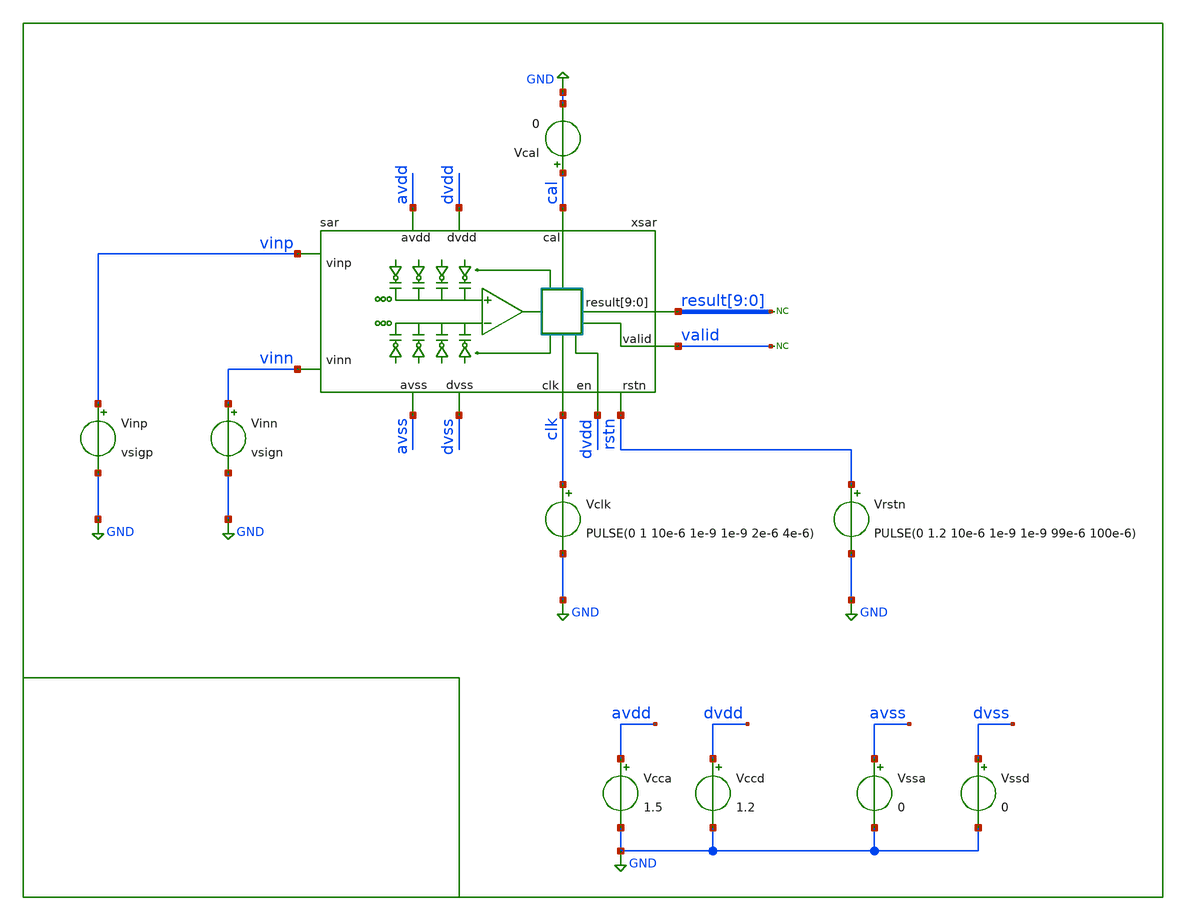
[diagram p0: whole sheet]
** sch_path: xschem/tb/sar_10b/tr_sar.sch
**.subckt tr_sar
Vssa avss GND 0
Vcca avdd GND 1.5
Vinn vinn GND vsign
Vinp vinp GND vsigp
Vclk clk GND PULSE(0 1 10e-6 1e-9 1e-9 2e-6 4e-6)
* noconn valid
Vcal cal GND 0
* noconn result[9:0]
xsar avdd dvdd dvss result[9] result[8] result[7] result[6] result[5] result[4] result[3] result[2]
+ result[1] result[0] vinn avss clk vinp dvdd valid cal rstn sar
Vrstn rstn GND PULSE(0 1.2 10e-6 1e-9 1e-9 99e-6 100e-6)
Vssd dvss GND 0
Vccd dvdd GND 1.2
**** begin user architecture code

.lib $::SKYWATER_MODELS/models/sky130.lib.spice tt
.include $::SKYWATER_STDCELLS/cells/inv/sky130_fd_sc_hd__inv_4.spice
.include $::SKYWATER_STDCELLS/cells/decap/sky130_fd_sc_hd__decap_8.spice
.include $::SKYWATER_STDCELLS/cells/decap/sky130_fd_sc_hd__decap_3.spice
.include $::SKYWATER_STDCELLS/cells/buf/sky130_fd_sc_hd__buf_1.spice
.include $::SKYWATER_STDCELLS/cells/inv/sky130_fd_sc_hd__inv_1.spice
.include $::SKYWATER_STDCELLS/cells/inv/sky130_fd_sc_hd__inv_2.spice
.include $::SKYWATER_STDCELLS/cells/tap/sky130_fd_sc_hd__tap_2.spice
 *-------------------------
* normal setup
*-------------------------
.options method = gear
.options gmin   = 1e-15
.options abstol = 1e-14
.options chtol  = 1e-18
.options reltol = 100e-6
*-------------------------

*-------------------------
* extracted logic setup
*-------------------------
*.options method = gear
*.options gmin   = 1e-12
*.options abstol = 1e-10
*.options chtol  = 1e-12
*.options reltol = 100e-3
*-------------------------


.ic v(xsar.vp)=0
.ic v(xsar.vn)=0
.ic v(xsar.outp)=0
.ic v(xsar.outn)=0
.ic v(xsar.comp)=0

.ic v(xsar.ctlp_0_)=0
.ic v(xsar.ctlp_1_)=0
.ic v(xsar.ctlp_2_)=0
.ic v(xsar.ctlp_3_)=0
.ic v(xsar.ctlp_4_)=0
.ic v(xsar.ctlp_5_)=0
.ic v(xsar.ctlp_6_)=0
.ic v(xsar.ctlp_7_)=0
.ic v(xsar.ctlp_8_)=0
.ic v(xsar.ctlp_9_)=0

.ic v(xsar.ctln_0_)=0
.ic v(xsar.ctln_1_)=0
.ic v(xsar.ctln_2_)=0
.ic v(xsar.ctln_3_)=0
.ic v(xsar.ctln_4_)=0
.ic v(xsar.ctln_5_)=0
.ic v(xsar.ctln_6_)=0
.ic v(xsar.ctln_7_)=0
.ic v(xsar.ctln_8_)=0
.ic v(xsar.ctln_9_)=0


*.include $::DESIGN_PATH/switches/bootstrapped_sw.sp
*.include $::DESIGN_PATH/sar_10b/dac/dac_mom.pex.sp
*.include $::DESIGN_PATH/sar_10b/sar/sar.pex.spice
*.include $::DESIGN_PATH/sar_10b/sar/sar_mom.pex.spice
*.include $::DESIGN_PATH/sar_10b/sar/sar_mim.pex.spice
*.include $::DESIGN_PATH/sar_10b/control/sarlogic.ext.spice
*.include $::DESIGN_PATH/sar_10b/sar/sar.pex.spice
.include $::DESIGN_PATH/sar_10b/sar/sar.ext.spice

.param MC_SWITCH=0
.param vin=0
.param vcm=0.75
.param vsigp="{vcm + vin/2}"
.param vsign="{vcm - vin/2}"

.tran 100e-9 68e-6 uic

.control

run

meas tran d0 find v(xsar.xlogic.res0) at=62.5e-6
meas tran d1 find v(xsar.xlogic.res1) at=62.5e-6
meas tran d2 find v(xsar.xlogic.res2) at=62.5e-6
meas tran d3 find v(xsar.xlogic.res3) at=62.5e-6
meas tran d4 find v(xsar.xlogic.res4) at=62.5e-6
meas tran d5 find v(xsar.xlogic.res5) at=62.5e-6
meas tran d6 find v(xsar.xlogic.res6) at=62.5e-6
meas tran d7 find v(xsar.xlogic.res7) at=62.5e-6
meas tran d8 find v(xsar.xlogic.res8) at=62.5e-6
meas tran d9 find v(xsar.xlogic.res9) at=62.5e-6

meas tran vpmax max xsar.vp
meas tran vpmin min xsar.vp
meas tran vpend find v(xsar.vp) at=62.5e-6

meas tran vnmax max xsar.vn
meas tran vnmin min xsar.vn
meas tran vnend find v(xsar.vn) at=62.5e-6

meas tran i_inp_max max(i_inp_abs)

* Current measurements
let i_inp_abs  = abs(vinp#branch)
let i_inn_abs  = abs(vinn#branch)
let i_vcca_abs = abs(vcca#branch)
let i_vccd_abs = abs(vccd#branch)

meas tran i_inp_max  max i_inp_abs   from=1u
meas tran i_inn_max  max i_inn_abs   from=1u
meas tran i_vcca_max max i_vcca_abs  from=1u
meas tran i_vccd_max max i_vccd_abs  from=1u


print i_inp_max
print i_inn_max
print i_vcca_max
print i_vccd_max

print d0
print d1
print d2
print d3
print d4
print d5
print d6
print d7
print d8
print d9

print vpmax
print vpmin

print vnmax
print vnmin

print vpend
print vnend

echo Simulation Finished
echo -------------------
shell date
echo -------------------

.endc

 * FET CORNERS
*.include $::SKYWATER_MODELS/corners/tt_all.spice
*.include $::SKYWATER_MODELS/corners/ff_all.spice
*.include $::SKYWATER_MODELS/corners/ss_all.spice
*.include $::SKYWATER_MODELS/corners/tt.spice
*.include $::SKYWATER_MODELS/corners/ff.spice
*.include $::SKYWATER_MODELS/corners/ss.spice
*.include $::SKYWATER_MODELS/corners/sf.spice
*.include $::SKYWATER_MODELS/corners/fs.spice

* TT + R + C
*.include $::SKYWATER_MODELS/corners/tt_rmax_cmax.spice
*.include $::SKYWATER_MODELS/corners/tt_rmin_cmin.spice
*.include $::SKYWATER_MODELS/corners/tt_rmax_cmin.spice
*.include $::SKYWATER_MODELS/corners/tt_rmin_cmax.spice

* FF + R + C
*.include $::SKYWATER_MODELS/corners/ff_rmax_cmax.spice
*.include $::SKYWATER_MODELS/corners/ff_rmin_cmin.spice
*.include $::SKYWATER_MODELS/corners/ff_rmax_cmin.spice
*.include $::SKYWATER_MODELS/corners/ff_rmin_cmax.spice


* SS + R + C
*.include $::SKYWATER_MODELS/corners/ss_rmax_cmax.spice
*.include $::SKYWATER_MODELS/corners/ss_rmin_cmin.spice
*.include $::SKYWATER_MODELS/corners/ss_rmax_cmin.spice
*.include $::SKYWATER_MODELS/corners/ss_rmin_cmax.spice

* SF + R + C
*.include $::SKYWATER_MODELS/corners/sf_rmax_cmax.spice
*.include $::SKYWATER_MODELS/corners/sf_rmin_cmin.spice
*.include $::SKYWATER_MODELS/corners/sf_rmax_cmin.spice
*.include $::SKYWATER_MODELS/corners/sf_rmin_cmax.spice

* FS + R + C
*.include $::SKYWATER_MODELS/corners/fs_rmax_cmax.spice
*.include $::SKYWATER_MODELS/corners/fs_rmin_cmin.spice
*.include $::SKYWATER_MODELS/corners/fs_rmax_cmin.spice
*.include $::SKYWATER_MODELS/corners/fs_rmin_cmax.spice

**** end user architecture code
**.ends
.GLOBAL GND
.end
